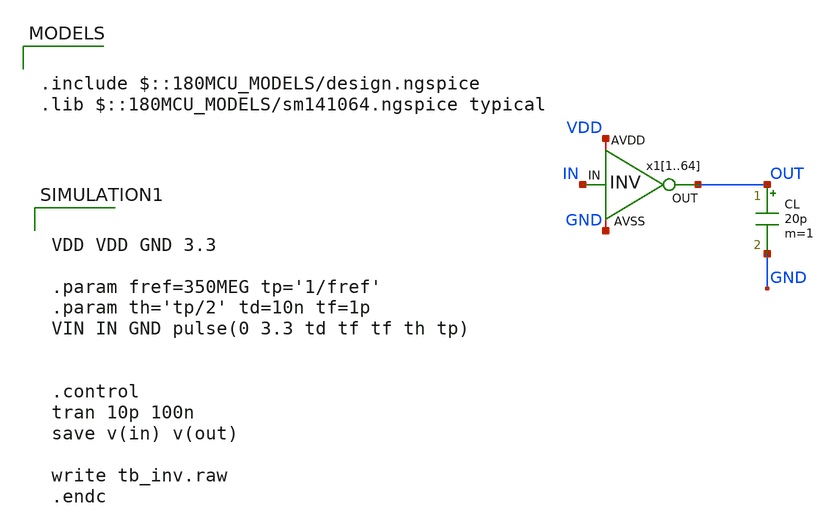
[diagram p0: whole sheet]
** sch_path: designs/libs/tb_analog/tb_inv/tb_inv.sch
**.subckt tb_inv
CL OUT GND 20p m=1
x11 VDD IN OUT GND inv
x12 VDD IN OUT GND inv
x13 VDD IN OUT GND inv
x14 VDD IN OUT GND inv
x15 VDD IN OUT GND inv
x16 VDD IN OUT GND inv
x17 VDD IN OUT GND inv
x18 VDD IN OUT GND inv
x19 VDD IN OUT GND inv
x110 VDD IN OUT GND inv
x111 VDD IN OUT GND inv
x112 VDD IN OUT GND inv
x113 VDD IN OUT GND inv
x114 VDD IN OUT GND inv
x115 VDD IN OUT GND inv
x116 VDD IN OUT GND inv
x117 VDD IN OUT GND inv
x118 VDD IN OUT GND inv
x119 VDD IN OUT GND inv
x120 VDD IN OUT GND inv
x121 VDD IN OUT GND inv
x122 VDD IN OUT GND inv
x123 VDD IN OUT GND inv
x124 VDD IN OUT GND inv
x125 VDD IN OUT GND inv
x126 VDD IN OUT GND inv
x127 VDD IN OUT GND inv
x128 VDD IN OUT GND inv
x129 VDD IN OUT GND inv
x130 VDD IN OUT GND inv
x131 VDD IN OUT GND inv
x132 VDD IN OUT GND inv
x133 VDD IN OUT GND inv
x134 VDD IN OUT GND inv
x135 VDD IN OUT GND inv
x136 VDD IN OUT GND inv
x137 VDD IN OUT GND inv
x138 VDD IN OUT GND inv
x139 VDD IN OUT GND inv
x140 VDD IN OUT GND inv
x141 VDD IN OUT GND inv
x142 VDD IN OUT GND inv
x143 VDD IN OUT GND inv
x144 VDD IN OUT GND inv
x145 VDD IN OUT GND inv
x146 VDD IN OUT GND inv
x147 VDD IN OUT GND inv
x148 VDD IN OUT GND inv
x149 VDD IN OUT GND inv
x150 VDD IN OUT GND inv
x151 VDD IN OUT GND inv
x152 VDD IN OUT GND inv
x153 VDD IN OUT GND inv
x154 VDD IN OUT GND inv
x155 VDD IN OUT GND inv
x156 VDD IN OUT GND inv
x157 VDD IN OUT GND inv
x158 VDD IN OUT GND inv
x159 VDD IN OUT GND inv
x160 VDD IN OUT GND inv
x161 VDD IN OUT GND inv
x162 VDD IN OUT GND inv
x163 VDD IN OUT GND inv
x164 VDD IN OUT GND inv
**** begin user architecture code


VDD VDD GND 3.3

.param fref=350MEG tp='1/fref'
.param th='tp/2' td=10n tf=1p
VIN IN GND pulse(0 3.3 td tf tf th tp)


.control
tran 10p 100n
save v(in) v(out)

write tb_inv.raw
.endc



.include $::180MCU_MODELS/design.ngspice
.lib $::180MCU_MODELS/sm141064.ngspice typical

**** end user architecture code
**.ends

* expanding   symbol:  libs/core_analog/inv/inv.sym # of pins=4
** sym_path: designs/libs/core_analog/inv/inv.sym
** sch_path: designs/libs/core_analog/inv/inv.sch
.subckt inv AVDD IN OUT AVSS
*.ipin IN
*.iopin AVDD
*.iopin AVSS
*.opin OUT
XM1 OUT IN AVDD AVDD pfet_03v3 L=0.28u W=0.9u nf=1 ad='int((nf+1)/2) * W/nf * 0.18u' as='int((nf+2)/2) * W/nf * 0.18u'
+ pd='2*int((nf+1)/2) * (W/nf + 0.18u)' ps='2*int((nf+2)/2) * (W/nf + 0.18u)' nrd='0.18u / W' nrs='0.18u / W'
+ sa=0 sb=0 sd=0 m=1
XM2 OUT IN AVSS AVSS nfet_03v3 L=0.28u W=0.3u nf=1 ad='int((nf+1)/2) * W/nf * 0.18u' as='int((nf+2)/2) * W/nf * 0.18u'
+ pd='2*int((nf+1)/2) * (W/nf + 0.18u)' ps='2*int((nf+2)/2) * (W/nf + 0.18u)' nrd='0.18u / W' nrs='0.18u / W'
+ sa=0 sb=0 sd=0 m=1
.ends

.end
